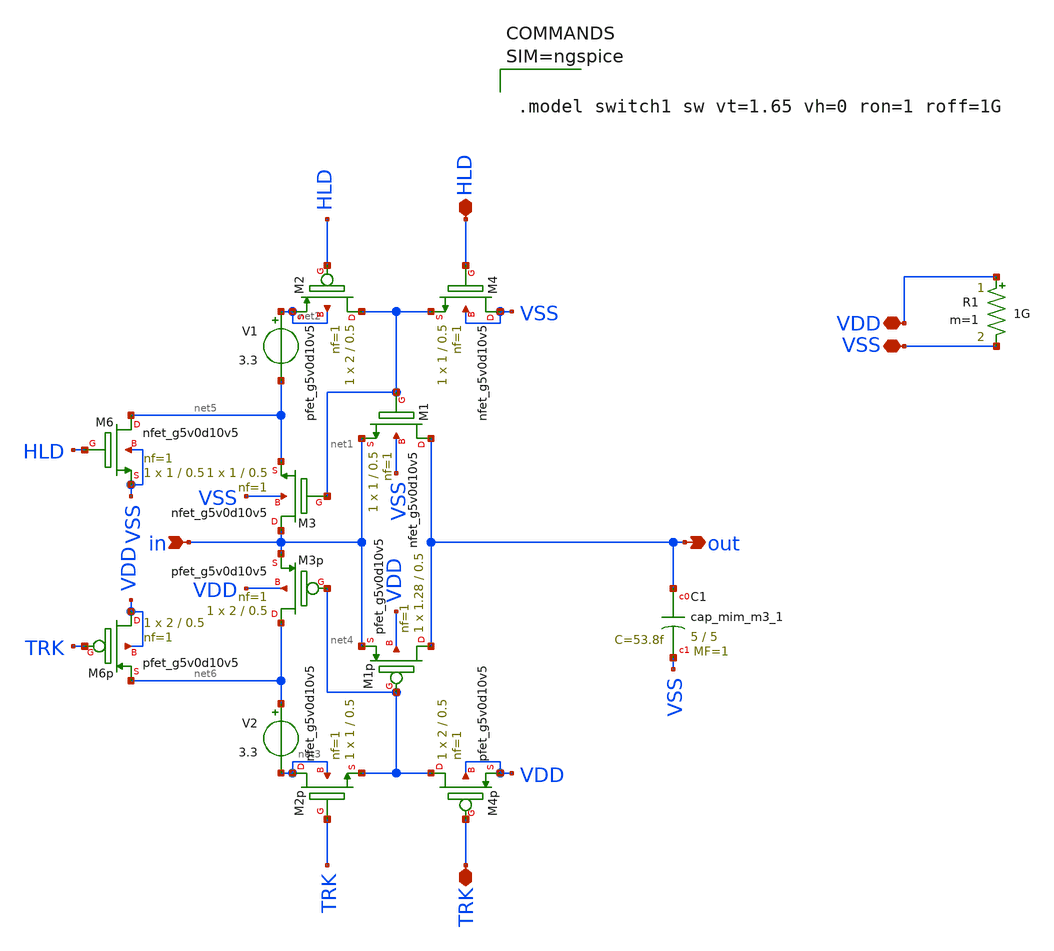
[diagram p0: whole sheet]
** sch_path: xschem/track_and_hold.sch
**.subckt track_and_hold VSS VDD in out TRK HLD
*.iopin VSS
*.iopin VDD
*.ipin in
*.opin out
*.iopin TRK
*.iopin HLD
XC1 out VSS sky130_fd_pr__cap_mim_m3_1 W=5 L=5 MF=1 m=1
V1 net2 net5 3.3
XM1 out net1 in VSS sky130_fd_pr__nfet_g5v0d10v5 L=0.5 W=1 nf=1 ad='int((nf+1)/2) * W/nf * 0.29' as='int((nf+2)/2) * W/nf * 0.29'
+ pd='2*int((nf+1)/2) * (W/nf + 0.29)' ps='2*int((nf+2)/2) * (W/nf + 0.29)' nrd='0.29 / W' nrs='0.29 / W'
+ sa=0 sb=0 sd=0 mult=1 m=1
R1 VDD VSS 1G m=1
V2 net6 net3 3.3
XM1p out net4 in VDD sky130_fd_pr__pfet_g5v0d10v5 L=0.5 W=1.28 nf=1 ad='int((nf+1)/2) * W/nf * 0.29'
+ as='int((nf+2)/2) * W/nf * 0.29' pd='2*int((nf+1)/2) * (W/nf + 0.29)' ps='2*int((nf+2)/2) * (W/nf + 0.29)'
+ nrd='0.29 / W' nrs='0.29 / W' sa=0 sb=0 sd=0 mult=1 m=1
XM4 VSS HLD net1 VSS sky130_fd_pr__nfet_g5v0d10v5 L=0.5 W=1 nf=1 ad='int((nf+1)/2) * W/nf * 0.29' as='int((nf+2)/2) * W/nf * 0.29'
+ pd='2*int((nf+1)/2) * (W/nf + 0.29)' ps='2*int((nf+2)/2) * (W/nf + 0.29)' nrd='0.29 / W' nrs='0.29 / W'
+ sa=0 sb=0 sd=0 mult=1 m=1
XM4p net4 TRK VDD VDD sky130_fd_pr__pfet_g5v0d10v5 L=0.5 W=2 nf=1 ad='int((nf+1)/2) * W/nf * 0.29' as='int((nf+2)/2) * W/nf * 0.29'
+ pd='2*int((nf+1)/2) * (W/nf + 0.29)' ps='2*int((nf+2)/2) * (W/nf + 0.29)' nrd='0.29 / W' nrs='0.29 / W'
+ sa=0 sb=0 sd=0 mult=1 m=1
XM2 net1 HLD net2 net2 sky130_fd_pr__pfet_g5v0d10v5 L=0.5 W=2 nf=1 ad='int((nf+1)/2) * W/nf * 0.29' as='int((nf+2)/2) * W/nf * 0.29'
+ pd='2*int((nf+1)/2) * (W/nf + 0.29)' ps='2*int((nf+2)/2) * (W/nf + 0.29)' nrd='0.29 / W' nrs='0.29 / W'
+ sa=0 sb=0 sd=0 mult=1 m=1
XM2p net3 TRK net4 net3 sky130_fd_pr__nfet_g5v0d10v5 L=0.5 W=1 nf=1 ad='int((nf+1)/2) * W/nf * 0.29'
+ as='int((nf+2)/2) * W/nf * 0.29' pd='2*int((nf+1)/2) * (W/nf + 0.29)' ps='2*int((nf+2)/2) * (W/nf + 0.29)'
+ nrd='0.29 / W' nrs='0.29 / W' sa=0 sb=0 sd=0 mult=1 m=1
XM3 in net1 net5 VSS sky130_fd_pr__nfet_g5v0d10v5 L=0.5 W=1 nf=1 ad='int((nf+1)/2) * W/nf * 0.29' as='int((nf+2)/2) * W/nf * 0.29'
+ pd='2*int((nf+1)/2) * (W/nf + 0.29)' ps='2*int((nf+2)/2) * (W/nf + 0.29)' nrd='0.29 / W' nrs='0.29 / W'
+ sa=0 sb=0 sd=0 mult=1 m=1
XM6 net5 HLD VSS VSS sky130_fd_pr__nfet_g5v0d10v5 L=0.5 W=1 nf=1 ad='int((nf+1)/2) * W/nf * 0.29' as='int((nf+2)/2) * W/nf * 0.29'
+ pd='2*int((nf+1)/2) * (W/nf + 0.29)' ps='2*int((nf+2)/2) * (W/nf + 0.29)' nrd='0.29 / W' nrs='0.29 / W'
+ sa=0 sb=0 sd=0 mult=1 m=1
XM3p net6 net4 in VDD sky130_fd_pr__pfet_g5v0d10v5 L=0.5 W=2 nf=1 ad='int((nf+1)/2) * W/nf * 0.29' as='int((nf+2)/2) * W/nf * 0.29'
+ pd='2*int((nf+1)/2) * (W/nf + 0.29)' ps='2*int((nf+2)/2) * (W/nf + 0.29)' nrd='0.29 / W' nrs='0.29 / W'
+ sa=0 sb=0 sd=0 mult=1 m=1
XM6p VDD TRK net6 VDD sky130_fd_pr__pfet_g5v0d10v5 L=0.5 W=2 nf=1 ad='int((nf+1)/2) * W/nf * 0.29' as='int((nf+2)/2) * W/nf * 0.29'
+ pd='2*int((nf+1)/2) * (W/nf + 0.29)' ps='2*int((nf+2)/2) * (W/nf + 0.29)' nrd='0.29 / W' nrs='0.29 / W'
+ sa=0 sb=0 sd=0 mult=1 m=1
**** begin user architecture code



.model switch1 sw vt=1.65 vh=0 ron=1 roff=1G



**** end user architecture code
**.ends
.end
